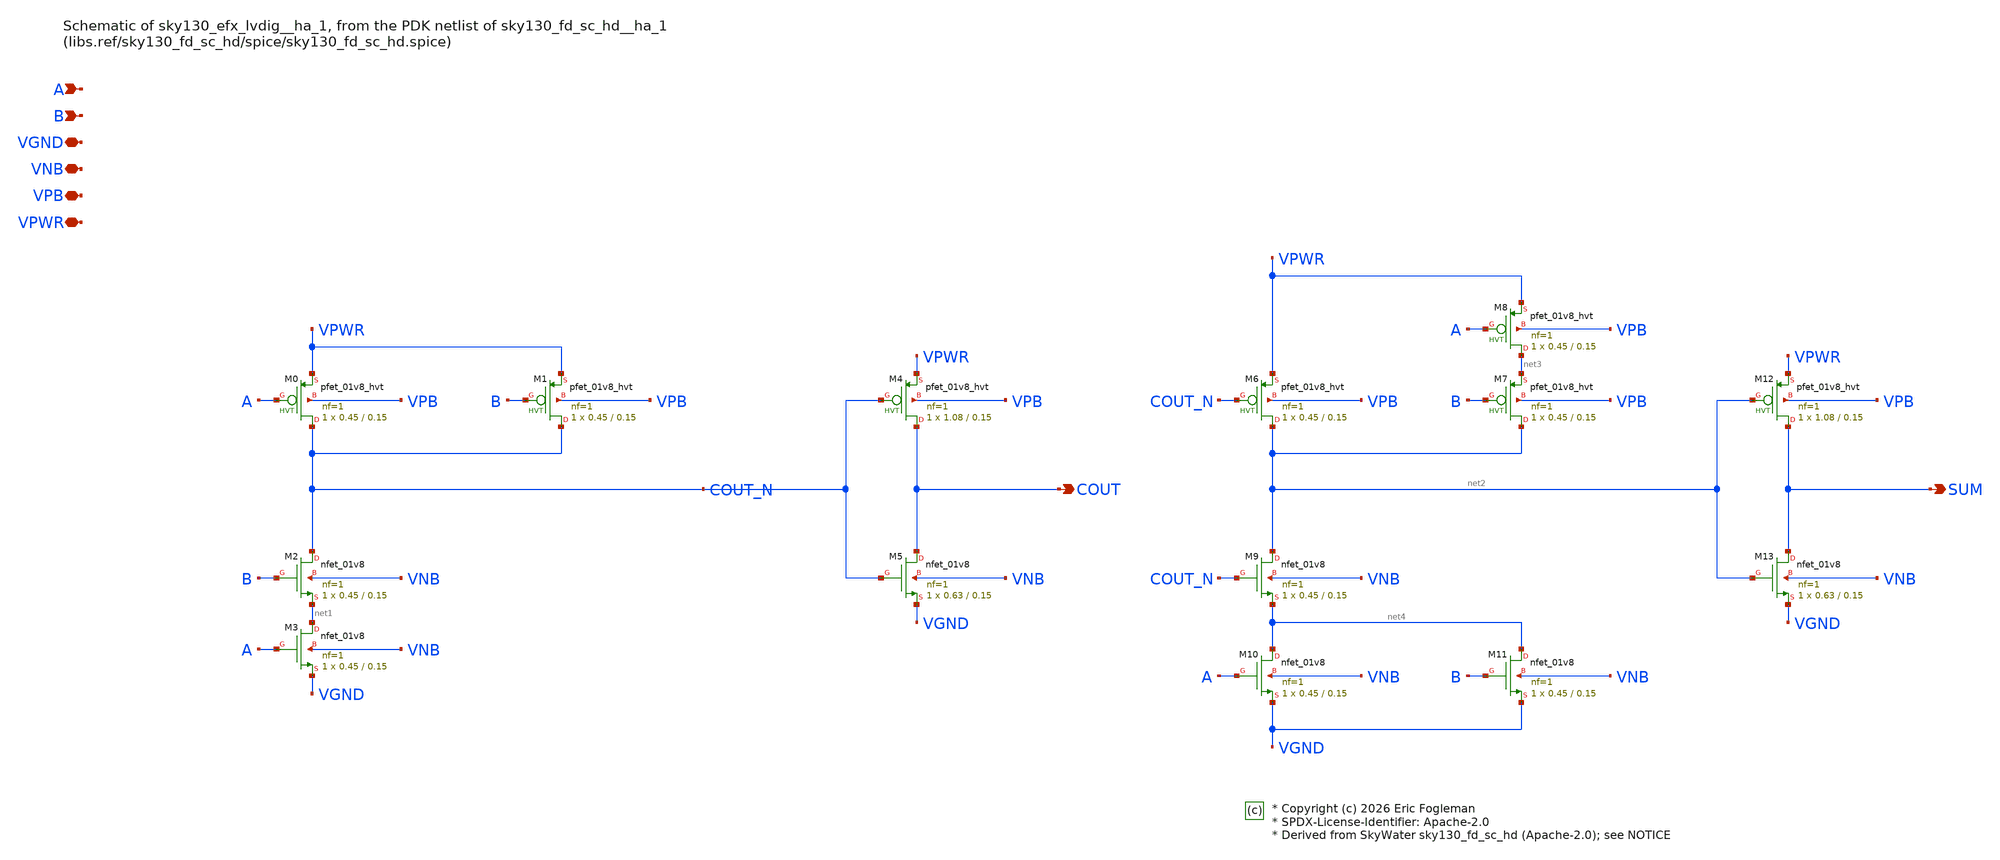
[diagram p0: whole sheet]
** sch_path: xschem/sky130_efx_lvdig__ha_1.sch

* Copyright (c) 2026 Eric Fogleman
* SPDX-License-Identifier: Apache-2.0
* Derived from SkyWater sky130_fd_sc_hd (Apache-2.0); see NOTICE

**.subckt sky130_efx_lvdig__ha_1 COUT SUM A B VGND VNB VPB VPWR
*.opin COUT
*.opin SUM
*.ipin A
*.ipin B
*.iopin VGND
*.iopin VNB
*.iopin VPB
*.iopin VPWR
XM0 COUT_N A VPWR VPB sky130_fd_pr__pfet_01v8_hvt L=0.15 W=0.45 nf=1 ad='int((1 + 1)/2) * 0.45 / 1 * 0.29'
+ as='int((1 + 2)/2) * 0.45 / 1 * 0.29' pd='2*int((1 + 1)/2) * (0.45 / 1 + 0.29)' ps='2*int((1 + 2)/2) * (0.45 / 1 + 0.29)'
+ nrd='0.29 / 0.45 ' nrs='0.29 / 0.45 ' sa=0 sb=0 sd=0 mult=1 m=1
XM1 COUT_N B VPWR VPB sky130_fd_pr__pfet_01v8_hvt L=0.15 W=0.45 nf=1 ad='int((1 + 1)/2) * 0.45 / 1 * 0.29'
+ as='int((1 + 2)/2) * 0.45 / 1 * 0.29' pd='2*int((1 + 1)/2) * (0.45 / 1 + 0.29)' ps='2*int((1 + 2)/2) * (0.45 / 1 + 0.29)'
+ nrd='0.29 / 0.45 ' nrs='0.29 / 0.45 ' sa=0 sb=0 sd=0 mult=1 m=1
XM2 COUT_N B net1 VNB sky130_fd_pr__nfet_01v8 L=0.15 W=0.45 nf=1 ad='int((1 + 1)/2) * 0.45 / 1 * 0.29'
+ as='int((1 + 2)/2) * 0.45 / 1 * 0.29' pd='2*int((1 + 1)/2) * (0.45 / 1 + 0.29)' ps='2*int((1 + 2)/2) * (0.45 / 1 + 0.29)'
+ nrd='0.29 / 0.45 ' nrs='0.29 / 0.45 ' sa=0 sb=0 sd=0 mult=1 m=1
XM3 net1 A VGND VNB sky130_fd_pr__nfet_01v8 L=0.15 W=0.45 nf=1 ad='int((1 + 1)/2) * 0.45 / 1 * 0.29'
+ as='int((1 + 2)/2) * 0.45 / 1 * 0.29' pd='2*int((1 + 1)/2) * (0.45 / 1 + 0.29)' ps='2*int((1 + 2)/2) * (0.45 / 1 + 0.29)'
+ nrd='0.29 / 0.45 ' nrs='0.29 / 0.45 ' sa=0 sb=0 sd=0 mult=1 m=1
XM4 COUT COUT_N VPWR VPB sky130_fd_pr__pfet_01v8_hvt L=0.15 W=1.08 nf=1 ad='int((1 + 1)/2) * 1.08 / 1 * 0.29'
+ as='int((1 + 2)/2) * 1.08 / 1 * 0.29' pd='2*int((1 + 1)/2) * (1.08 / 1 + 0.29)' ps='2*int((1 + 2)/2) * (1.08 / 1 + 0.29)'
+ nrd='0.29 / 1.08 ' nrs='0.29 / 1.08 ' sa=0 sb=0 sd=0 mult=1 m=1
XM5 COUT COUT_N VGND VNB sky130_fd_pr__nfet_01v8 L=0.15 W=0.63 nf=1 ad='int((1 + 1)/2) * 0.63 / 1 * 0.29'
+ as='int((1 + 2)/2) * 0.63 / 1 * 0.29' pd='2*int((1 + 1)/2) * (0.63 / 1 + 0.29)' ps='2*int((1 + 2)/2) * (0.63 / 1 + 0.29)'
+ nrd='0.29 / 0.63 ' nrs='0.29 / 0.63 ' sa=0 sb=0 sd=0 mult=1 m=1
XM6 net2 COUT_N VPWR VPB sky130_fd_pr__pfet_01v8_hvt L=0.15 W=0.45 nf=1 ad='int((1 + 1)/2) * 0.45 / 1 * 0.29'
+ as='int((1 + 2)/2) * 0.45 / 1 * 0.29' pd='2*int((1 + 1)/2) * (0.45 / 1 + 0.29)' ps='2*int((1 + 2)/2) * (0.45 / 1 + 0.29)'
+ nrd='0.29 / 0.45 ' nrs='0.29 / 0.45 ' sa=0 sb=0 sd=0 mult=1 m=1
XM7 net2 B net3 VPB sky130_fd_pr__pfet_01v8_hvt L=0.15 W=0.45 nf=1 ad='int((1 + 1)/2) * 0.45 / 1 * 0.29'
+ as='int((1 + 2)/2) * 0.45 / 1 * 0.29' pd='2*int((1 + 1)/2) * (0.45 / 1 + 0.29)' ps='2*int((1 + 2)/2) * (0.45 / 1 + 0.29)'
+ nrd='0.29 / 0.45 ' nrs='0.29 / 0.45 ' sa=0 sb=0 sd=0 mult=1 m=1
XM8 net3 A VPWR VPB sky130_fd_pr__pfet_01v8_hvt L=0.15 W=0.45 nf=1 ad='int((1 + 1)/2) * 0.45 / 1 * 0.29'
+ as='int((1 + 2)/2) * 0.45 / 1 * 0.29' pd='2*int((1 + 1)/2) * (0.45 / 1 + 0.29)' ps='2*int((1 + 2)/2) * (0.45 / 1 + 0.29)'
+ nrd='0.29 / 0.45 ' nrs='0.29 / 0.45 ' sa=0 sb=0 sd=0 mult=1 m=1
XM9 net2 COUT_N net4 VNB sky130_fd_pr__nfet_01v8 L=0.15 W=0.45 nf=1 ad='int((1 + 1)/2) * 0.45 / 1 * 0.29'
+ as='int((1 + 2)/2) * 0.45 / 1 * 0.29' pd='2*int((1 + 1)/2) * (0.45 / 1 + 0.29)' ps='2*int((1 + 2)/2) * (0.45 / 1 + 0.29)'
+ nrd='0.29 / 0.45 ' nrs='0.29 / 0.45 ' sa=0 sb=0 sd=0 mult=1 m=1
XM10 net4 A VGND VNB sky130_fd_pr__nfet_01v8 L=0.15 W=0.45 nf=1 ad='int((1 + 1)/2) * 0.45 / 1 * 0.29'
+ as='int((1 + 2)/2) * 0.45 / 1 * 0.29' pd='2*int((1 + 1)/2) * (0.45 / 1 + 0.29)' ps='2*int((1 + 2)/2) * (0.45 / 1 + 0.29)'
+ nrd='0.29 / 0.45 ' nrs='0.29 / 0.45 ' sa=0 sb=0 sd=0 mult=1 m=1
XM11 net4 B VGND VNB sky130_fd_pr__nfet_01v8 L=0.15 W=0.45 nf=1 ad='int((1 + 1)/2) * 0.45 / 1 * 0.29'
+ as='int((1 + 2)/2) * 0.45 / 1 * 0.29' pd='2*int((1 + 1)/2) * (0.45 / 1 + 0.29)' ps='2*int((1 + 2)/2) * (0.45 / 1 + 0.29)'
+ nrd='0.29 / 0.45 ' nrs='0.29 / 0.45 ' sa=0 sb=0 sd=0 mult=1 m=1
XM12 SUM net2 VPWR VPB sky130_fd_pr__pfet_01v8_hvt L=0.15 W=1.08 nf=1 ad='int((1 + 1)/2) * 1.08 / 1 * 0.29'
+ as='int((1 + 2)/2) * 1.08 / 1 * 0.29' pd='2*int((1 + 1)/2) * (1.08 / 1 + 0.29)' ps='2*int((1 + 2)/2) * (1.08 / 1 + 0.29)'
+ nrd='0.29 / 1.08 ' nrs='0.29 / 1.08 ' sa=0 sb=0 sd=0 mult=1 m=1
XM13 SUM net2 VGND VNB sky130_fd_pr__nfet_01v8 L=0.15 W=0.63 nf=1 ad='int((1 + 1)/2) * 0.63 / 1 * 0.29'
+ as='int((1 + 2)/2) * 0.63 / 1 * 0.29' pd='2*int((1 + 1)/2) * (0.63 / 1 + 0.29)' ps='2*int((1 + 2)/2) * (0.63 / 1 + 0.29)'
+ nrd='0.29 / 0.63 ' nrs='0.29 / 0.63 ' sa=0 sb=0 sd=0 mult=1 m=1
**.ends
.end
